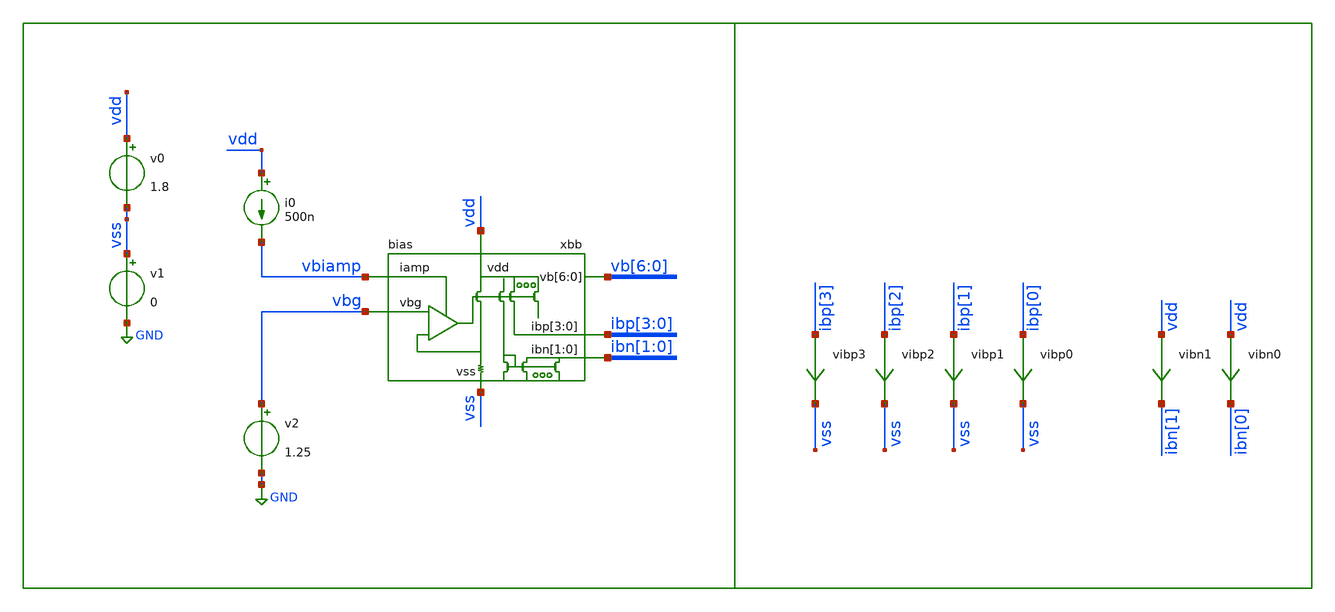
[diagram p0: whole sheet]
** sch_path: xschem/tb/bias/dc_bias_standalone.sch
**.subckt dc_bias_standalone
v0 vdd vss 1.8
v1 vss GND 0
xbb vbiamp vbg ibp[3] ibp[2] ibp[1] ibp[0] ibn[1] ibn[0] vdd vss vb[6] vb[5] vb[4] vb[3] vb[2] vb[1]
+ vb[0] bias
vibp3 ibp[3] vss 0
.save i(vibp3)
vibp1 ibp[1] vss 0
.save i(vibp1)
vibp2 ibp[2] vss 0
.save i(vibp2)
vibp0 ibp[0] vss 0
.save i(vibp0)
vibn1 vdd ibn[1] 0
.save i(vibn1)
vibn0 vdd ibn[0] 0
.save i(vibn0)
v2 vbg GND 1.25
i0 vdd vbiamp 500n
**** begin user architecture code

.control
.param MC_SWITCH=0

save all
op

echo -----------------
print vb_0_
print vb_1_
print vb_2_
print vb_3_
print vb_4_
print vb_5_
print vb_6_

print vibp0#branch
print vibp1#branch
print vibp2#branch
print vibp3#branch

print vibn0#branch
print vibn1#branch

print v.xbb.vbase#branch
print v.xbb.vm1#branch
print v.xbb.vm1#branch
echo -----------------

*dc temp -10 75 0.1
*plot vibp0#branch
*plot vibp1#branch
*plot vbg
* tran 1n 10u
.endc


 .include $::SKYWATER_STDCELLS/cells/inv/sky130_fd_sc_hd__inv_1.spice

* FET CORNERS
.include $::SKYWATER_MODELS/corners/tt.spice
*.include $::SKYWATER_MODELS/corners/ff.spice
*.include $::SKYWATER_MODELS/corners/ss.spice
*.include $::SKYWATER_MODELS/corners/sf.spice
*.include $::SKYWATER_MODELS/corners/fs.spice

* TT + R + C
*.include $::SKYWATER_MODELS/corners/tt_rmax_cmax.spice
*.include $::SKYWATER_MODELS/corners/tt_rmin_cmin.spice
*.include $::SKYWATER_MODELS/corners/tt_rmax_cmin.spice
*.include $::SKYWATER_MODELS/corners/tt_rmin_cmax.spice

* FF + R + C
*.include $::SKYWATER_MODELS/corners/ff_rmax_cmax.spice
*.include $::SKYWATER_MODELS/corners/ff_rmin_cmin.spice
*.include $::SKYWATER_MODELS/corners/ff_rmax_cmin.spice
*.include $::SKYWATER_MODELS/corners/ff_rmin_cmax.spice


* SS + R + C
*.include $::SKYWATER_MODELS/corners/ss_rmax_cmax.spice
*.include $::SKYWATER_MODELS/corners/ss_rmin_cmin.spice
*.include $::SKYWATER_MODELS/corners/ss_rmax_cmin.spice
*.include $::SKYWATER_MODELS/corners/ss_rmin_cmax.spice

* SF + R + C
*.include $::SKYWATER_MODELS/corners/sf_rmax_cmax.spice
*.include $::SKYWATER_MODELS/corners/sf_rmin_cmin.spice
*.include $::SKYWATER_MODELS/corners/sf_rmax_cmin.spice
*.include $::SKYWATER_MODELS/corners/sf_rmin_cmax.spice

* FS + R + C
*.include $::SKYWATER_MODELS/corners/fs_rmax_cmax.spice
*.include $::SKYWATER_MODELS/corners/fs_rmin_cmin.spice
*.include $::SKYWATER_MODELS/corners/fs_rmax_cmin.spice
*.include $::SKYWATER_MODELS/corners/fs_rmin_cmax.spice

**** end user architecture code
**.ends

* expanding   symbol:  bias/bias.sym # of pins=7
** sym_path: xschem/bias/bias.sym
** sch_path: xschem/bias/bias.sch
.subckt bias iamp vbg ibp[3] ibp[2] ibp[1] ibp[0] ibn[1] ibn[0] vdd vss vb[6] vb[5] vb[4] vb[3]
+ vb[2] vb[1] vb[0]
*.ipin vbg
*.ipin iamp
*.iopin vdd
*.iopin ibp[3],ibp[2],ibp[1],ibp[0]
*.iopin ibn[1],ibn[0]
*.iopin vb[6],vb[5],vb[4],vb[3],vb[2],vb[1],vb[0]
*.iopin vss
x1 vdd gate fb vbg vss iamp bias_amp
XMP2[1] gate_cas gate net1[1] vdd sky130_fd_pr__pfet_01v8_lvt L=2 W=0.5 nf=1 ad='int((nf+1)/2) * W/nf * 0.29'
+ as='int((nf+2)/2) * W/nf * 0.29' pd='2*int((nf+1)/2) * (W/nf + 0.29)' ps='2*int((nf+2)/2) * (W/nf + 0.29)'
+ nrd='0.29 / W' nrs='0.29 / W' sa=0 sb=0 sd=0 mult=1 m=1
XMP2[0] gate_cas gate net1[0] vdd sky130_fd_pr__pfet_01v8_lvt L=2 W=0.5 nf=1 ad='int((nf+1)/2) * W/nf * 0.29'
+ as='int((nf+2)/2) * W/nf * 0.29' pd='2*int((nf+1)/2) * (W/nf + 0.29)' ps='2*int((nf+2)/2) * (W/nf + 0.29)'
+ nrd='0.29 / W' nrs='0.29 / W' sa=0 sb=0 sd=0 mult=1 m=1
XM1 fb gate vdd vdd sky130_fd_pr__pfet_01v8_lvt L=2 W=0.5 nf=1 ad='int((nf+1)/2) * W/nf * 0.29' as='int((nf+2)/2) * W/nf * 0.29'
+ pd='2*int((nf+1)/2) * (W/nf + 0.29)' ps='2*int((nf+2)/2) * (W/nf + 0.29)' nrd='0.29 / W' nrs='0.29 / W'
+ sa=0 sb=0 sd=0 mult=8 m=8
XMPS2[1] net1[1] gate vdd vdd sky130_fd_pr__pfet_01v8_lvt L=2 W=0.5 nf=1 ad='int((nf+1)/2) * W/nf * 0.29'
+ as='int((nf+2)/2) * W/nf * 0.29' pd='2*int((nf+1)/2) * (W/nf + 0.29)' ps='2*int((nf+2)/2) * (W/nf + 0.29)'
+ nrd='0.29 / W' nrs='0.29 / W' sa=0 sb=0 sd=0 mult=1 m=1
XMPS2[0] net1[0] gate vdd vdd sky130_fd_pr__pfet_01v8_lvt L=2 W=0.5 nf=1 ad='int((nf+1)/2) * W/nf * 0.29'
+ as='int((nf+2)/2) * W/nf * 0.29' pd='2*int((nf+1)/2) * (W/nf + 0.29)' ps='2*int((nf+2)/2) * (W/nf + 0.29)'
+ nrd='0.29 / W' nrs='0.29 / W' sa=0 sb=0 sd=0 mult=1 m=1
XMP4[1] ibp[1] gate net2[1] vdd sky130_fd_pr__pfet_01v8_lvt L=2 W=0.5 nf=1 ad='int((nf+1)/2) * W/nf * 0.29'
+ as='int((nf+2)/2) * W/nf * 0.29' pd='2*int((nf+1)/2) * (W/nf + 0.29)' ps='2*int((nf+2)/2) * (W/nf + 0.29)'
+ nrd='0.29 / W' nrs='0.29 / W' sa=0 sb=0 sd=0 mult=1 m=1
XMP4[0] ibp[1] gate net2[0] vdd sky130_fd_pr__pfet_01v8_lvt L=2 W=0.5 nf=1 ad='int((nf+1)/2) * W/nf * 0.29'
+ as='int((nf+2)/2) * W/nf * 0.29' pd='2*int((nf+1)/2) * (W/nf + 0.29)' ps='2*int((nf+2)/2) * (W/nf + 0.29)'
+ nrd='0.29 / W' nrs='0.29 / W' sa=0 sb=0 sd=0 mult=1 m=1
XMPS4[1] net2[1] gate vdd vdd sky130_fd_pr__pfet_01v8_lvt L=2 W=0.5 nf=1 ad='int((nf+1)/2) * W/nf * 0.29'
+ as='int((nf+2)/2) * W/nf * 0.29' pd='2*int((nf+1)/2) * (W/nf + 0.29)' ps='2*int((nf+2)/2) * (W/nf + 0.29)'
+ nrd='0.29 / W' nrs='0.29 / W' sa=0 sb=0 sd=0 mult=1 m=1
XMPS4[0] net2[0] gate vdd vdd sky130_fd_pr__pfet_01v8_lvt L=2 W=0.5 nf=1 ad='int((nf+1)/2) * W/nf * 0.29'
+ as='int((nf+2)/2) * W/nf * 0.29' pd='2*int((nf+1)/2) * (W/nf + 0.29)' ps='2*int((nf+2)/2) * (W/nf + 0.29)'
+ nrd='0.29 / W' nrs='0.29 / W' sa=0 sb=0 sd=0 mult=1 m=1
XMP5[1] ibp[2] gate net3[1] vdd sky130_fd_pr__pfet_01v8_lvt L=2 W=0.5 nf=1 ad='int((nf+1)/2) * W/nf * 0.29'
+ as='int((nf+2)/2) * W/nf * 0.29' pd='2*int((nf+1)/2) * (W/nf + 0.29)' ps='2*int((nf+2)/2) * (W/nf + 0.29)'
+ nrd='0.29 / W' nrs='0.29 / W' sa=0 sb=0 sd=0 mult=1 m=1
XMP5[0] ibp[2] gate net3[0] vdd sky130_fd_pr__pfet_01v8_lvt L=2 W=0.5 nf=1 ad='int((nf+1)/2) * W/nf * 0.29'
+ as='int((nf+2)/2) * W/nf * 0.29' pd='2*int((nf+1)/2) * (W/nf + 0.29)' ps='2*int((nf+2)/2) * (W/nf + 0.29)'
+ nrd='0.29 / W' nrs='0.29 / W' sa=0 sb=0 sd=0 mult=1 m=1
XMPS5[1] net3[1] gate vdd vdd sky130_fd_pr__pfet_01v8_lvt L=2 W=0.5 nf=1 ad='int((nf+1)/2) * W/nf * 0.29'
+ as='int((nf+2)/2) * W/nf * 0.29' pd='2*int((nf+1)/2) * (W/nf + 0.29)' ps='2*int((nf+2)/2) * (W/nf + 0.29)'
+ nrd='0.29 / W' nrs='0.29 / W' sa=0 sb=0 sd=0 mult=1 m=1
XMPS5[0] net3[0] gate vdd vdd sky130_fd_pr__pfet_01v8_lvt L=2 W=0.5 nf=1 ad='int((nf+1)/2) * W/nf * 0.29'
+ as='int((nf+2)/2) * W/nf * 0.29' pd='2*int((nf+1)/2) * (W/nf + 0.29)' ps='2*int((nf+2)/2) * (W/nf + 0.29)'
+ nrd='0.29 / W' nrs='0.29 / W' sa=0 sb=0 sd=0 mult=1 m=1
XMP6[1] ibp[3] gate net4[1] vdd sky130_fd_pr__pfet_01v8_lvt L=2 W=0.5 nf=1 ad='int((nf+1)/2) * W/nf * 0.29'
+ as='int((nf+2)/2) * W/nf * 0.29' pd='2*int((nf+1)/2) * (W/nf + 0.29)' ps='2*int((nf+2)/2) * (W/nf + 0.29)'
+ nrd='0.29 / W' nrs='0.29 / W' sa=0 sb=0 sd=0 mult=1 m=1
XMP6[0] ibp[3] gate net4[0] vdd sky130_fd_pr__pfet_01v8_lvt L=2 W=0.5 nf=1 ad='int((nf+1)/2) * W/nf * 0.29'
+ as='int((nf+2)/2) * W/nf * 0.29' pd='2*int((nf+1)/2) * (W/nf + 0.29)' ps='2*int((nf+2)/2) * (W/nf + 0.29)'
+ nrd='0.29 / W' nrs='0.29 / W' sa=0 sb=0 sd=0 mult=1 m=1
XMPS6[1] net4[1] gate vdd vdd sky130_fd_pr__pfet_01v8_lvt L=2 W=0.5 nf=1 ad='int((nf+1)/2) * W/nf * 0.29'
+ as='int((nf+2)/2) * W/nf * 0.29' pd='2*int((nf+1)/2) * (W/nf + 0.29)' ps='2*int((nf+2)/2) * (W/nf + 0.29)'
+ nrd='0.29 / W' nrs='0.29 / W' sa=0 sb=0 sd=0 mult=1 m=1
XMPS6[0] net4[0] gate vdd vdd sky130_fd_pr__pfet_01v8_lvt L=2 W=0.5 nf=1 ad='int((nf+1)/2) * W/nf * 0.29'
+ as='int((nf+2)/2) * W/nf * 0.29' pd='2*int((nf+1)/2) * (W/nf + 0.29)' ps='2*int((nf+2)/2) * (W/nf + 0.29)'
+ nrd='0.29 / W' nrs='0.29 / W' sa=0 sb=0 sd=0 mult=1 m=1
XMP3[3] ibp[0] gate net5[3] vdd sky130_fd_pr__pfet_01v8_lvt L=2 W=0.5 nf=1 ad='int((nf+1)/2) * W/nf * 0.29'
+ as='int((nf+2)/2) * W/nf * 0.29' pd='2*int((nf+1)/2) * (W/nf + 0.29)' ps='2*int((nf+2)/2) * (W/nf + 0.29)'
+ nrd='0.29 / W' nrs='0.29 / W' sa=0 sb=0 sd=0 mult=1 m=1
XMP3[2] ibp[0] gate net5[2] vdd sky130_fd_pr__pfet_01v8_lvt L=2 W=0.5 nf=1 ad='int((nf+1)/2) * W/nf * 0.29'
+ as='int((nf+2)/2) * W/nf * 0.29' pd='2*int((nf+1)/2) * (W/nf + 0.29)' ps='2*int((nf+2)/2) * (W/nf + 0.29)'
+ nrd='0.29 / W' nrs='0.29 / W' sa=0 sb=0 sd=0 mult=1 m=1
XMP3[1] ibp[0] gate net5[1] vdd sky130_fd_pr__pfet_01v8_lvt L=2 W=0.5 nf=1 ad='int((nf+1)/2) * W/nf * 0.29'
+ as='int((nf+2)/2) * W/nf * 0.29' pd='2*int((nf+1)/2) * (W/nf + 0.29)' ps='2*int((nf+2)/2) * (W/nf + 0.29)'
+ nrd='0.29 / W' nrs='0.29 / W' sa=0 sb=0 sd=0 mult=1 m=1
XMP3[0] ibp[0] gate net5[0] vdd sky130_fd_pr__pfet_01v8_lvt L=2 W=0.5 nf=1 ad='int((nf+1)/2) * W/nf * 0.29'
+ as='int((nf+2)/2) * W/nf * 0.29' pd='2*int((nf+1)/2) * (W/nf + 0.29)' ps='2*int((nf+2)/2) * (W/nf + 0.29)'
+ nrd='0.29 / W' nrs='0.29 / W' sa=0 sb=0 sd=0 mult=1 m=1
XMPS3[3] net5[3] gate vdd vdd sky130_fd_pr__pfet_01v8_lvt L=2 W=0.5 nf=1 ad='int((nf+1)/2) * W/nf * 0.29'
+ as='int((nf+2)/2) * W/nf * 0.29' pd='2*int((nf+1)/2) * (W/nf + 0.29)' ps='2*int((nf+2)/2) * (W/nf + 0.29)'
+ nrd='0.29 / W' nrs='0.29 / W' sa=0 sb=0 sd=0 mult=1 m=1
XMPS3[2] net5[2] gate vdd vdd sky130_fd_pr__pfet_01v8_lvt L=2 W=0.5 nf=1 ad='int((nf+1)/2) * W/nf * 0.29'
+ as='int((nf+2)/2) * W/nf * 0.29' pd='2*int((nf+1)/2) * (W/nf + 0.29)' ps='2*int((nf+2)/2) * (W/nf + 0.29)'
+ nrd='0.29 / W' nrs='0.29 / W' sa=0 sb=0 sd=0 mult=1 m=1
XMPS3[1] net5[1] gate vdd vdd sky130_fd_pr__pfet_01v8_lvt L=2 W=0.5 nf=1 ad='int((nf+1)/2) * W/nf * 0.29'
+ as='int((nf+2)/2) * W/nf * 0.29' pd='2*int((nf+1)/2) * (W/nf + 0.29)' ps='2*int((nf+2)/2) * (W/nf + 0.29)'
+ nrd='0.29 / W' nrs='0.29 / W' sa=0 sb=0 sd=0 mult=1 m=1
XMPS3[0] net5[0] gate vdd vdd sky130_fd_pr__pfet_01v8_lvt L=2 W=0.5 nf=1 ad='int((nf+1)/2) * W/nf * 0.29'
+ as='int((nf+2)/2) * W/nf * 0.29' pd='2*int((nf+1)/2) * (W/nf + 0.29)' ps='2*int((nf+2)/2) * (W/nf + 0.29)'
+ nrd='0.29 / W' nrs='0.29 / W' sa=0 sb=0 sd=0 mult=1 m=1
XMNS2[3] gate_n gate_n vss vss sky130_fd_pr__nfet_01v8_lvt L=2 W=1 nf=1 ad='int((nf+1)/2) * W/nf * 0.29'
+ as='int((nf+2)/2) * W/nf * 0.29' pd='2*int((nf+1)/2) * (W/nf + 0.29)' ps='2*int((nf+2)/2) * (W/nf + 0.29)'
+ nrd='0.29 / W' nrs='0.29 / W' sa=0 sb=0 sd=0 mult=1 m=1
XMNS2[2] gate_n gate_n vss vss sky130_fd_pr__nfet_01v8_lvt L=2 W=1 nf=1 ad='int((nf+1)/2) * W/nf * 0.29'
+ as='int((nf+2)/2) * W/nf * 0.29' pd='2*int((nf+1)/2) * (W/nf + 0.29)' ps='2*int((nf+2)/2) * (W/nf + 0.29)'
+ nrd='0.29 / W' nrs='0.29 / W' sa=0 sb=0 sd=0 mult=1 m=1
XMNS2[1] gate_n gate_n vss vss sky130_fd_pr__nfet_01v8_lvt L=2 W=1 nf=1 ad='int((nf+1)/2) * W/nf * 0.29'
+ as='int((nf+2)/2) * W/nf * 0.29' pd='2*int((nf+1)/2) * (W/nf + 0.29)' ps='2*int((nf+2)/2) * (W/nf + 0.29)'
+ nrd='0.29 / W' nrs='0.29 / W' sa=0 sb=0 sd=0 mult=1 m=1
XMNS2[0] gate_n gate_n vss vss sky130_fd_pr__nfet_01v8_lvt L=2 W=1 nf=1 ad='int((nf+1)/2) * W/nf * 0.29'
+ as='int((nf+2)/2) * W/nf * 0.29' pd='2*int((nf+1)/2) * (W/nf + 0.29)' ps='2*int((nf+2)/2) * (W/nf + 0.29)'
+ nrd='0.29 / W' nrs='0.29 / W' sa=0 sb=0 sd=0 mult=1 m=1
XMNS3[3] net6[3] gate_n vss vss sky130_fd_pr__nfet_01v8_lvt L=2 W=1 nf=1 ad='int((nf+1)/2) * W/nf * 0.29'
+ as='int((nf+2)/2) * W/nf * 0.29' pd='2*int((nf+1)/2) * (W/nf + 0.29)' ps='2*int((nf+2)/2) * (W/nf + 0.29)'
+ nrd='0.29 / W' nrs='0.29 / W' sa=0 sb=0 sd=0 mult=1 m=1
XMNS3[2] net6[2] gate_n vss vss sky130_fd_pr__nfet_01v8_lvt L=2 W=1 nf=1 ad='int((nf+1)/2) * W/nf * 0.29'
+ as='int((nf+2)/2) * W/nf * 0.29' pd='2*int((nf+1)/2) * (W/nf + 0.29)' ps='2*int((nf+2)/2) * (W/nf + 0.29)'
+ nrd='0.29 / W' nrs='0.29 / W' sa=0 sb=0 sd=0 mult=1 m=1
XMNS3[1] net6[1] gate_n vss vss sky130_fd_pr__nfet_01v8_lvt L=2 W=1 nf=1 ad='int((nf+1)/2) * W/nf * 0.29'
+ as='int((nf+2)/2) * W/nf * 0.29' pd='2*int((nf+1)/2) * (W/nf + 0.29)' ps='2*int((nf+2)/2) * (W/nf + 0.29)'
+ nrd='0.29 / W' nrs='0.29 / W' sa=0 sb=0 sd=0 mult=1 m=1
XMNS3[0] net6[0] gate_n vss vss sky130_fd_pr__nfet_01v8_lvt L=2 W=1 nf=1 ad='int((nf+1)/2) * W/nf * 0.29'
+ as='int((nf+2)/2) * W/nf * 0.29' pd='2*int((nf+1)/2) * (W/nf + 0.29)' ps='2*int((nf+2)/2) * (W/nf + 0.29)'
+ nrd='0.29 / W' nrs='0.29 / W' sa=0 sb=0 sd=0 mult=1 m=1
XMNS4[3] net7[3] gate_n vss vss sky130_fd_pr__nfet_01v8_lvt L=2 W=1 nf=1 ad='int((nf+1)/2) * W/nf * 0.29'
+ as='int((nf+2)/2) * W/nf * 0.29' pd='2*int((nf+1)/2) * (W/nf + 0.29)' ps='2*int((nf+2)/2) * (W/nf + 0.29)'
+ nrd='0.29 / W' nrs='0.29 / W' sa=0 sb=0 sd=0 mult=1 m=1
XMNS4[2] net7[2] gate_n vss vss sky130_fd_pr__nfet_01v8_lvt L=2 W=1 nf=1 ad='int((nf+1)/2) * W/nf * 0.29'
+ as='int((nf+2)/2) * W/nf * 0.29' pd='2*int((nf+1)/2) * (W/nf + 0.29)' ps='2*int((nf+2)/2) * (W/nf + 0.29)'
+ nrd='0.29 / W' nrs='0.29 / W' sa=0 sb=0 sd=0 mult=1 m=1
XMNS4[1] net7[1] gate_n vss vss sky130_fd_pr__nfet_01v8_lvt L=2 W=1 nf=1 ad='int((nf+1)/2) * W/nf * 0.29'
+ as='int((nf+2)/2) * W/nf * 0.29' pd='2*int((nf+1)/2) * (W/nf + 0.29)' ps='2*int((nf+2)/2) * (W/nf + 0.29)'
+ nrd='0.29 / W' nrs='0.29 / W' sa=0 sb=0 sd=0 mult=1 m=1
XMNS4[0] net7[0] gate_n vss vss sky130_fd_pr__nfet_01v8_lvt L=2 W=1 nf=1 ad='int((nf+1)/2) * W/nf * 0.29'
+ as='int((nf+2)/2) * W/nf * 0.29' pd='2*int((nf+1)/2) * (W/nf + 0.29)' ps='2*int((nf+2)/2) * (W/nf + 0.29)'
+ nrd='0.29 / W' nrs='0.29 / W' sa=0 sb=0 sd=0 mult=1 m=1
XMN2[3] gate_cas gate_cas gate_n vss sky130_fd_pr__nfet_01v8_lvt L=2 W=1 nf=1 ad='int((nf+1)/2) * W/nf * 0.29'
+ as='int((nf+2)/2) * W/nf * 0.29' pd='2*int((nf+1)/2) * (W/nf + 0.29)' ps='2*int((nf+2)/2) * (W/nf + 0.29)'
+ nrd='0.29 / W' nrs='0.29 / W' sa=0 sb=0 sd=0 mult=1 m=1
XMN2[2] gate_cas gate_cas gate_n vss sky130_fd_pr__nfet_01v8_lvt L=2 W=1 nf=1 ad='int((nf+1)/2) * W/nf * 0.29'
+ as='int((nf+2)/2) * W/nf * 0.29' pd='2*int((nf+1)/2) * (W/nf + 0.29)' ps='2*int((nf+2)/2) * (W/nf + 0.29)'
+ nrd='0.29 / W' nrs='0.29 / W' sa=0 sb=0 sd=0 mult=1 m=1
XMN2[1] gate_cas gate_cas gate_n vss sky130_fd_pr__nfet_01v8_lvt L=2 W=1 nf=1 ad='int((nf+1)/2) * W/nf * 0.29'
+ as='int((nf+2)/2) * W/nf * 0.29' pd='2*int((nf+1)/2) * (W/nf + 0.29)' ps='2*int((nf+2)/2) * (W/nf + 0.29)'
+ nrd='0.29 / W' nrs='0.29 / W' sa=0 sb=0 sd=0 mult=1 m=1
XMN2[0] gate_cas gate_cas gate_n vss sky130_fd_pr__nfet_01v8_lvt L=2 W=1 nf=1 ad='int((nf+1)/2) * W/nf * 0.29'
+ as='int((nf+2)/2) * W/nf * 0.29' pd='2*int((nf+1)/2) * (W/nf + 0.29)' ps='2*int((nf+2)/2) * (W/nf + 0.29)'
+ nrd='0.29 / W' nrs='0.29 / W' sa=0 sb=0 sd=0 mult=1 m=1
XMN3[3] ibn[0] gate_cas net6[3] vss sky130_fd_pr__nfet_01v8_lvt L=2 W=1 nf=1 ad='int((nf+1)/2) * W/nf * 0.29'
+ as='int((nf+2)/2) * W/nf * 0.29' pd='2*int((nf+1)/2) * (W/nf + 0.29)' ps='2*int((nf+2)/2) * (W/nf + 0.29)'
+ nrd='0.29 / W' nrs='0.29 / W' sa=0 sb=0 sd=0 mult=1 m=1
XMN3[2] ibn[0] gate_cas net6[2] vss sky130_fd_pr__nfet_01v8_lvt L=2 W=1 nf=1 ad='int((nf+1)/2) * W/nf * 0.29'
+ as='int((nf+2)/2) * W/nf * 0.29' pd='2*int((nf+1)/2) * (W/nf + 0.29)' ps='2*int((nf+2)/2) * (W/nf + 0.29)'
+ nrd='0.29 / W' nrs='0.29 / W' sa=0 sb=0 sd=0 mult=1 m=1
XMN3[1] ibn[0] gate_cas net6[1] vss sky130_fd_pr__nfet_01v8_lvt L=2 W=1 nf=1 ad='int((nf+1)/2) * W/nf * 0.29'
+ as='int((nf+2)/2) * W/nf * 0.29' pd='2*int((nf+1)/2) * (W/nf + 0.29)' ps='2*int((nf+2)/2) * (W/nf + 0.29)'
+ nrd='0.29 / W' nrs='0.29 / W' sa=0 sb=0 sd=0 mult=1 m=1
XMN3[0] ibn[0] gate_cas net6[0] vss sky130_fd_pr__nfet_01v8_lvt L=2 W=1 nf=1 ad='int((nf+1)/2) * W/nf * 0.29'
+ as='int((nf+2)/2) * W/nf * 0.29' pd='2*int((nf+1)/2) * (W/nf + 0.29)' ps='2*int((nf+2)/2) * (W/nf + 0.29)'
+ nrd='0.29 / W' nrs='0.29 / W' sa=0 sb=0 sd=0 mult=1 m=1
XMN4[3] ibn[1] gate_cas net7[3] vss sky130_fd_pr__nfet_01v8_lvt L=2 W=1 nf=1 ad='int((nf+1)/2) * W/nf * 0.29'
+ as='int((nf+2)/2) * W/nf * 0.29' pd='2*int((nf+1)/2) * (W/nf + 0.29)' ps='2*int((nf+2)/2) * (W/nf + 0.29)'
+ nrd='0.29 / W' nrs='0.29 / W' sa=0 sb=0 sd=0 mult=1 m=1
XMN4[2] ibn[1] gate_cas net7[2] vss sky130_fd_pr__nfet_01v8_lvt L=2 W=1 nf=1 ad='int((nf+1)/2) * W/nf * 0.29'
+ as='int((nf+2)/2) * W/nf * 0.29' pd='2*int((nf+1)/2) * (W/nf + 0.29)' ps='2*int((nf+2)/2) * (W/nf + 0.29)'
+ nrd='0.29 / W' nrs='0.29 / W' sa=0 sb=0 sd=0 mult=1 m=1
XMN4[1] ibn[1] gate_cas net7[1] vss sky130_fd_pr__nfet_01v8_lvt L=2 W=1 nf=1 ad='int((nf+1)/2) * W/nf * 0.29'
+ as='int((nf+2)/2) * W/nf * 0.29' pd='2*int((nf+1)/2) * (W/nf + 0.29)' ps='2*int((nf+2)/2) * (W/nf + 0.29)'
+ nrd='0.29 / W' nrs='0.29 / W' sa=0 sb=0 sd=0 mult=1 m=1
XMN4[0] ibn[1] gate_cas net7[0] vss sky130_fd_pr__nfet_01v8_lvt L=2 W=1 nf=1 ad='int((nf+1)/2) * W/nf * 0.29'
+ as='int((nf+2)/2) * W/nf * 0.29' pd='2*int((nf+1)/2) * (W/nf + 0.29)' ps='2*int((nf+2)/2) * (W/nf + 0.29)'
+ nrd='0.29 / W' nrs='0.29 / W' sa=0 sb=0 sd=0 mult=1 m=1
XC1 gate fb sky130_fd_pr__cap_mim_m3_1 W=5 L=5 MF=8 m=8
XR1 fb net8 vss sky130_fd_pr__res_xhigh_po W=0.69 L=25.8 mult=1 m=1
XR2 net8 vb[0] vss sky130_fd_pr__res_xhigh_po W=0.69 L=25.8 mult=1 m=1
XR3 vb[0] net9 vss sky130_fd_pr__res_xhigh_po W=0.69 L=25.8 mult=1 m=1
XR4 net9 vb[1] vss sky130_fd_pr__res_xhigh_po W=0.69 L=25.8 mult=1 m=1
XR5 vb[2] net11 vss sky130_fd_pr__res_xhigh_po W=0.69 L=25.8 mult=1 m=1
XR6 net11 vb[1] vss sky130_fd_pr__res_xhigh_po W=0.69 L=25.8 mult=1 m=1
XR7 vb[3] net10 vss sky130_fd_pr__res_xhigh_po W=0.69 L=25.8 mult=1 m=1
XR8 net10 vb[2] vss sky130_fd_pr__res_xhigh_po W=0.69 L=25.8 mult=1 m=1
XR9 vb[3] net12 vss sky130_fd_pr__res_xhigh_po W=0.69 L=25.8 mult=1 m=1
XR10 net12 vb[4] vss sky130_fd_pr__res_xhigh_po W=0.69 L=25.8 mult=1 m=1
XR11 vb[4] net13 vss sky130_fd_pr__res_xhigh_po W=0.69 L=25.8 mult=1 m=1
XR12 net13 vb[5] vss sky130_fd_pr__res_xhigh_po W=0.69 L=25.8 mult=1 m=1
XR13 vb[6] net15 vss sky130_fd_pr__res_xhigh_po W=0.69 L=25.8 mult=1 m=1
XR14 net15 vb[5] vss sky130_fd_pr__res_xhigh_po W=0.69 L=25.8 mult=1 m=1
XR15 vss net14 vss sky130_fd_pr__res_xhigh_po W=0.69 L=25.8 mult=1 m=1
XR16 net14 vb[6] vss sky130_fd_pr__res_xhigh_po W=0.69 L=25.8 mult=1 m=1
XMP1 vdd gate vdd vdd sky130_fd_pr__pfet_01v8_lvt L=2 W=0.5 nf=1 ad='int((nf+1)/2) * W/nf * 0.29' as='int((nf+2)/2) * W/nf * 0.29'
+ pd='2*int((nf+1)/2) * (W/nf + 0.29)' ps='2*int((nf+2)/2) * (W/nf + 0.29)' nrd='0.29 / W' nrs='0.29 / W'
+ sa=0 sb=0 sd=0 mult=24 m=24
XMDUM[7] vss gate_cas vss vss sky130_fd_pr__nfet_01v8_lvt L=2 W=1 nf=1 ad='int((nf+1)/2) * W/nf * 0.29'
+ as='int((nf+2)/2) * W/nf * 0.29' pd='2*int((nf+1)/2) * (W/nf + 0.29)' ps='2*int((nf+2)/2) * (W/nf + 0.29)'
+ nrd='0.29 / W' nrs='0.29 / W' sa=0 sb=0 sd=0 mult=1 m=1
XMDUM[6] vss gate_cas vss vss sky130_fd_pr__nfet_01v8_lvt L=2 W=1 nf=1 ad='int((nf+1)/2) * W/nf * 0.29'
+ as='int((nf+2)/2) * W/nf * 0.29' pd='2*int((nf+1)/2) * (W/nf + 0.29)' ps='2*int((nf+2)/2) * (W/nf + 0.29)'
+ nrd='0.29 / W' nrs='0.29 / W' sa=0 sb=0 sd=0 mult=1 m=1
XMDUM[5] vss gate_cas vss vss sky130_fd_pr__nfet_01v8_lvt L=2 W=1 nf=1 ad='int((nf+1)/2) * W/nf * 0.29'
+ as='int((nf+2)/2) * W/nf * 0.29' pd='2*int((nf+1)/2) * (W/nf + 0.29)' ps='2*int((nf+2)/2) * (W/nf + 0.29)'
+ nrd='0.29 / W' nrs='0.29 / W' sa=0 sb=0 sd=0 mult=1 m=1
XMDUM[4] vss gate_cas vss vss sky130_fd_pr__nfet_01v8_lvt L=2 W=1 nf=1 ad='int((nf+1)/2) * W/nf * 0.29'
+ as='int((nf+2)/2) * W/nf * 0.29' pd='2*int((nf+1)/2) * (W/nf + 0.29)' ps='2*int((nf+2)/2) * (W/nf + 0.29)'
+ nrd='0.29 / W' nrs='0.29 / W' sa=0 sb=0 sd=0 mult=1 m=1
XMDUM[3] vss gate_cas vss vss sky130_fd_pr__nfet_01v8_lvt L=2 W=1 nf=1 ad='int((nf+1)/2) * W/nf * 0.29'
+ as='int((nf+2)/2) * W/nf * 0.29' pd='2*int((nf+1)/2) * (W/nf + 0.29)' ps='2*int((nf+2)/2) * (W/nf + 0.29)'
+ nrd='0.29 / W' nrs='0.29 / W' sa=0 sb=0 sd=0 mult=1 m=1
XMDUM[2] vss gate_cas vss vss sky130_fd_pr__nfet_01v8_lvt L=2 W=1 nf=1 ad='int((nf+1)/2) * W/nf * 0.29'
+ as='int((nf+2)/2) * W/nf * 0.29' pd='2*int((nf+1)/2) * (W/nf + 0.29)' ps='2*int((nf+2)/2) * (W/nf + 0.29)'
+ nrd='0.29 / W' nrs='0.29 / W' sa=0 sb=0 sd=0 mult=1 m=1
XMDUM[1] vss gate_cas vss vss sky130_fd_pr__nfet_01v8_lvt L=2 W=1 nf=1 ad='int((nf+1)/2) * W/nf * 0.29'
+ as='int((nf+2)/2) * W/nf * 0.29' pd='2*int((nf+1)/2) * (W/nf + 0.29)' ps='2*int((nf+2)/2) * (W/nf + 0.29)'
+ nrd='0.29 / W' nrs='0.29 / W' sa=0 sb=0 sd=0 mult=1 m=1
XMDUM[0] vss gate_cas vss vss sky130_fd_pr__nfet_01v8_lvt L=2 W=1 nf=1 ad='int((nf+1)/2) * W/nf * 0.29'
+ as='int((nf+2)/2) * W/nf * 0.29' pd='2*int((nf+1)/2) * (W/nf + 0.29)' ps='2*int((nf+2)/2) * (W/nf + 0.29)'
+ nrd='0.29 / W' nrs='0.29 / W' sa=0 sb=0 sd=0 mult=1 m=1
XMDUM_1[3] vss gate_n vss vss sky130_fd_pr__nfet_01v8_lvt L=2 W=1 nf=1 ad='int((nf+1)/2) * W/nf * 0.29'
+ as='int((nf+2)/2) * W/nf * 0.29' pd='2*int((nf+1)/2) * (W/nf + 0.29)' ps='2*int((nf+2)/2) * (W/nf + 0.29)'
+ nrd='0.29 / W' nrs='0.29 / W' sa=0 sb=0 sd=0 mult=1 m=1
XMDUM_1[2] vss gate_n vss vss sky130_fd_pr__nfet_01v8_lvt L=2 W=1 nf=1 ad='int((nf+1)/2) * W/nf * 0.29'
+ as='int((nf+2)/2) * W/nf * 0.29' pd='2*int((nf+1)/2) * (W/nf + 0.29)' ps='2*int((nf+2)/2) * (W/nf + 0.29)'
+ nrd='0.29 / W' nrs='0.29 / W' sa=0 sb=0 sd=0 mult=1 m=1
XMDUM_1[1] vss gate_n vss vss sky130_fd_pr__nfet_01v8_lvt L=2 W=1 nf=1 ad='int((nf+1)/2) * W/nf * 0.29'
+ as='int((nf+2)/2) * W/nf * 0.29' pd='2*int((nf+1)/2) * (W/nf + 0.29)' ps='2*int((nf+2)/2) * (W/nf + 0.29)'
+ nrd='0.29 / W' nrs='0.29 / W' sa=0 sb=0 sd=0 mult=1 m=1
XMDUM_1[0] vss gate_n vss vss sky130_fd_pr__nfet_01v8_lvt L=2 W=1 nf=1 ad='int((nf+1)/2) * W/nf * 0.29'
+ as='int((nf+2)/2) * W/nf * 0.29' pd='2*int((nf+1)/2) * (W/nf + 0.29)' ps='2*int((nf+2)/2) * (W/nf + 0.29)'
+ nrd='0.29 / W' nrs='0.29 / W' sa=0 sb=0 sd=0 mult=1 m=1
XMDUM1[3] ibn[0] gate_cas ibn[0] vss sky130_fd_pr__nfet_01v8_lvt L=2 W=1 nf=1 ad='int((nf+1)/2) * W/nf * 0.29'
+ as='int((nf+2)/2) * W/nf * 0.29' pd='2*int((nf+1)/2) * (W/nf + 0.29)' ps='2*int((nf+2)/2) * (W/nf + 0.29)'
+ nrd='0.29 / W' nrs='0.29 / W' sa=0 sb=0 sd=0 mult=1 m=1
XMDUM1[2] ibn[0] gate_cas ibn[0] vss sky130_fd_pr__nfet_01v8_lvt L=2 W=1 nf=1 ad='int((nf+1)/2) * W/nf * 0.29'
+ as='int((nf+2)/2) * W/nf * 0.29' pd='2*int((nf+1)/2) * (W/nf + 0.29)' ps='2*int((nf+2)/2) * (W/nf + 0.29)'
+ nrd='0.29 / W' nrs='0.29 / W' sa=0 sb=0 sd=0 mult=1 m=1
XMDUM1[1] ibn[0] gate_cas ibn[0] vss sky130_fd_pr__nfet_01v8_lvt L=2 W=1 nf=1 ad='int((nf+1)/2) * W/nf * 0.29'
+ as='int((nf+2)/2) * W/nf * 0.29' pd='2*int((nf+1)/2) * (W/nf + 0.29)' ps='2*int((nf+2)/2) * (W/nf + 0.29)'
+ nrd='0.29 / W' nrs='0.29 / W' sa=0 sb=0 sd=0 mult=1 m=1
XMDUM1[0] ibn[0] gate_cas ibn[0] vss sky130_fd_pr__nfet_01v8_lvt L=2 W=1 nf=1 ad='int((nf+1)/2) * W/nf * 0.29'
+ as='int((nf+2)/2) * W/nf * 0.29' pd='2*int((nf+1)/2) * (W/nf + 0.29)' ps='2*int((nf+2)/2) * (W/nf + 0.29)'
+ nrd='0.29 / W' nrs='0.29 / W' sa=0 sb=0 sd=0 mult=1 m=1
XMDUM2[3] ibn[1] gate_cas ibn[1] vss sky130_fd_pr__nfet_01v8_lvt L=2 W=1 nf=1 ad='int((nf+1)/2) * W/nf * 0.29'
+ as='int((nf+2)/2) * W/nf * 0.29' pd='2*int((nf+1)/2) * (W/nf + 0.29)' ps='2*int((nf+2)/2) * (W/nf + 0.29)'
+ nrd='0.29 / W' nrs='0.29 / W' sa=0 sb=0 sd=0 mult=1 m=1
XMDUM2[2] ibn[1] gate_cas ibn[1] vss sky130_fd_pr__nfet_01v8_lvt L=2 W=1 nf=1 ad='int((nf+1)/2) * W/nf * 0.29'
+ as='int((nf+2)/2) * W/nf * 0.29' pd='2*int((nf+1)/2) * (W/nf + 0.29)' ps='2*int((nf+2)/2) * (W/nf + 0.29)'
+ nrd='0.29 / W' nrs='0.29 / W' sa=0 sb=0 sd=0 mult=1 m=1
XMDUM2[1] ibn[1] gate_cas ibn[1] vss sky130_fd_pr__nfet_01v8_lvt L=2 W=1 nf=1 ad='int((nf+1)/2) * W/nf * 0.29'
+ as='int((nf+2)/2) * W/nf * 0.29' pd='2*int((nf+1)/2) * (W/nf + 0.29)' ps='2*int((nf+2)/2) * (W/nf + 0.29)'
+ nrd='0.29 / W' nrs='0.29 / W' sa=0 sb=0 sd=0 mult=1 m=1
XMDUM2[0] ibn[1] gate_cas ibn[1] vss sky130_fd_pr__nfet_01v8_lvt L=2 W=1 nf=1 ad='int((nf+1)/2) * W/nf * 0.29'
+ as='int((nf+2)/2) * W/nf * 0.29' pd='2*int((nf+1)/2) * (W/nf + 0.29)' ps='2*int((nf+2)/2) * (W/nf + 0.29)'
+ nrd='0.29 / W' nrs='0.29 / W' sa=0 sb=0 sd=0 mult=1 m=1
XMDUM3[3] gate_cas gate_cas gate_cas vss sky130_fd_pr__nfet_01v8_lvt L=2 W=1 nf=1 ad='int((nf+1)/2) * W/nf * 0.29'
+ as='int((nf+2)/2) * W/nf * 0.29' pd='2*int((nf+1)/2) * (W/nf + 0.29)' ps='2*int((nf+2)/2) * (W/nf + 0.29)'
+ nrd='0.29 / W' nrs='0.29 / W' sa=0 sb=0 sd=0 mult=1 m=1
XMDUM3[2] gate_cas gate_cas gate_cas vss sky130_fd_pr__nfet_01v8_lvt L=2 W=1 nf=1 ad='int((nf+1)/2) * W/nf * 0.29'
+ as='int((nf+2)/2) * W/nf * 0.29' pd='2*int((nf+1)/2) * (W/nf + 0.29)' ps='2*int((nf+2)/2) * (W/nf + 0.29)'
+ nrd='0.29 / W' nrs='0.29 / W' sa=0 sb=0 sd=0 mult=1 m=1
XMDUM3[1] gate_cas gate_cas gate_cas vss sky130_fd_pr__nfet_01v8_lvt L=2 W=1 nf=1 ad='int((nf+1)/2) * W/nf * 0.29'
+ as='int((nf+2)/2) * W/nf * 0.29' pd='2*int((nf+1)/2) * (W/nf + 0.29)' ps='2*int((nf+2)/2) * (W/nf + 0.29)'
+ nrd='0.29 / W' nrs='0.29 / W' sa=0 sb=0 sd=0 mult=1 m=1
XMDUM3[0] gate_cas gate_cas gate_cas vss sky130_fd_pr__nfet_01v8_lvt L=2 W=1 nf=1 ad='int((nf+1)/2) * W/nf * 0.29'
+ as='int((nf+2)/2) * W/nf * 0.29' pd='2*int((nf+1)/2) * (W/nf + 0.29)' ps='2*int((nf+2)/2) * (W/nf + 0.29)'
+ nrd='0.29 / W' nrs='0.29 / W' sa=0 sb=0 sd=0 mult=1 m=1
XR17[1] vss vss vss sky130_fd_pr__res_xhigh_po W=0.69 L=25.8 mult=1 m=1
XR17[0] vss vss vss sky130_fd_pr__res_xhigh_po W=0.69 L=25.8 mult=1 m=1
.ends


* expanding   symbol:  bias/bias_amp.sym # of pins=6
** sym_path: xschem/bias/bias_amp.sym
** sch_path: xschem/bias/bias_amp.sch
.subckt bias_amp vdd out inp inn vss bias
*.iopin vdd
*.iopin bias
*.ipin inp
*.ipin inn
*.opin out
*.iopin vss
XM3 mirr mirr vdd vdd sky130_fd_pr__pfet_01v8_lvt L=10 W=0.5 nf=1 ad='int((nf+1)/2) * W/nf * 0.29' as='int((nf+2)/2) * W/nf * 0.29'
+ pd='2*int((nf+1)/2) * (W/nf + 0.29)' ps='2*int((nf+2)/2) * (W/nf + 0.29)' nrd='0.29 / W' nrs='0.29 / W'
+ sa=0 sb=0 sd=0 mult=4 m=4
XM4 out mirr vdd vdd sky130_fd_pr__pfet_01v8_lvt L=10 W=0.5 nf=1 ad='int((nf+1)/2) * W/nf * 0.29' as='int((nf+2)/2) * W/nf * 0.29'
+ pd='2*int((nf+1)/2) * (W/nf + 0.29)' ps='2*int((nf+2)/2) * (W/nf + 0.29)' nrd='0.29 / W' nrs='0.29 / W'
+ sa=0 sb=0 sd=0 mult=4 m=4
XM1 mirr inp diff vss sky130_fd_pr__nfet_01v8_lvt L=8 W=0.5 nf=1 ad='int((nf+1)/2) * W/nf * 0.29' as='int((nf+2)/2) * W/nf * 0.29'
+ pd='2*int((nf+1)/2) * (W/nf + 0.29)' ps='2*int((nf+2)/2) * (W/nf + 0.29)' nrd='0.29 / W' nrs='0.29 / W'
+ sa=0 sb=0 sd=0 mult=4 m=4
XM2 out inn diff vss sky130_fd_pr__nfet_01v8_lvt L=8 W=0.5 nf=1 ad='int((nf+1)/2) * W/nf * 0.29' as='int((nf+2)/2) * W/nf * 0.29'
+ pd='2*int((nf+1)/2) * (W/nf + 0.29)' ps='2*int((nf+2)/2) * (W/nf + 0.29)' nrd='0.29 / W' nrs='0.29 / W'
+ sa=0 sb=0 sd=0 mult=4 m=4
XM5 net1 bias vss vss sky130_fd_pr__nfet_01v8_lvt L=4 W=0.5 nf=1 ad='int((nf+1)/2) * W/nf * 0.29' as='int((nf+2)/2) * W/nf * 0.29'
+ pd='2*int((nf+1)/2) * (W/nf + 0.29)' ps='2*int((nf+2)/2) * (W/nf + 0.29)' nrd='0.29 / W' nrs='0.29 / W'
+ sa=0 sb=0 sd=0 mult=4 m=4
XM6 bias bias vss vss sky130_fd_pr__nfet_01v8_lvt L=4 W=0.5 nf=1 ad='int((nf+1)/2) * W/nf * 0.29' as='int((nf+2)/2) * W/nf * 0.29'
+ pd='2*int((nf+1)/2) * (W/nf + 0.29)' ps='2*int((nf+2)/2) * (W/nf + 0.29)' nrd='0.29 / W' nrs='0.29 / W'
+ sa=0 sb=0 sd=0 mult=8 m=8
XM5s diff bias net1 vss sky130_fd_pr__nfet_01v8_lvt L=4 W=0.5 nf=1 ad='int((nf+1)/2) * W/nf * 0.29' as='int((nf+2)/2) * W/nf * 0.29'
+ pd='2*int((nf+1)/2) * (W/nf + 0.29)' ps='2*int((nf+2)/2) * (W/nf + 0.29)' nrd='0.29 / W' nrs='0.29 / W'
+ sa=0 sb=0 sd=0 mult=4 m=4
.ends

.GLOBAL GND
.end
